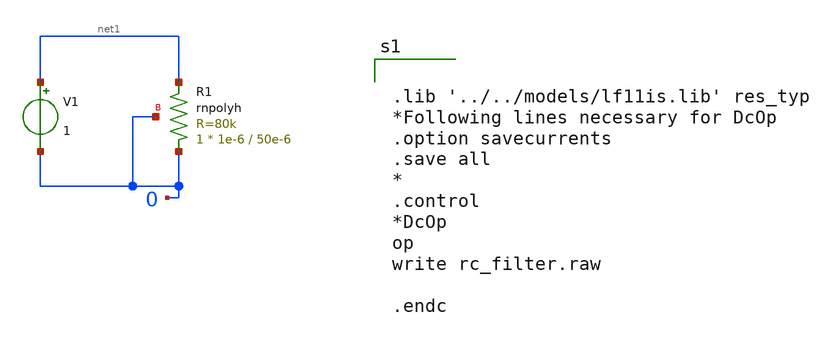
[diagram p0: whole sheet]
** sch_path: test_rnpolyh.sch
**.subckt test_rnpolyh
V1 net1 0 1
XR1 0 net1 0 rnpolyh w=1e-6 l=50e-6 m=1
**** begin user architecture code


.lib '../../models/lf11is.lib' res_typ
*Following lines necessary for DcOp
.option savecurrents
.save all
*
.control
*DcOp
op
write rc_filter.raw

.endc


**** end user architecture code
**.ends
.end
